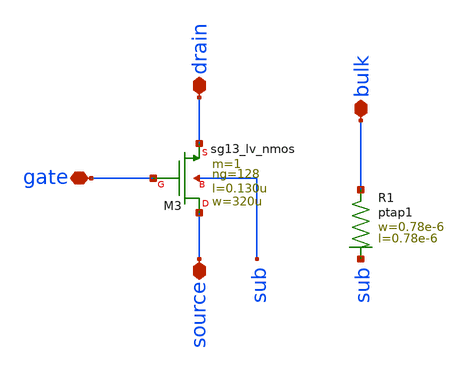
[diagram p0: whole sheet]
** sch_path: ts_pr_May2024/design_data/xschem/nmos128.sch
**.subckt nmos128 drain source bulk gate
*.iopin drain
*.iopin source
*.iopin bulk
*.iopin gate
XR1 bulk sub ptap1 R=262.8 w=0.78e-6 l=0.78e-6
XM3 source gate drain sub sg13_lv_nmos w=320u l=0.130u ng=128 m=1 mm_ok=1
**.ends
.end
